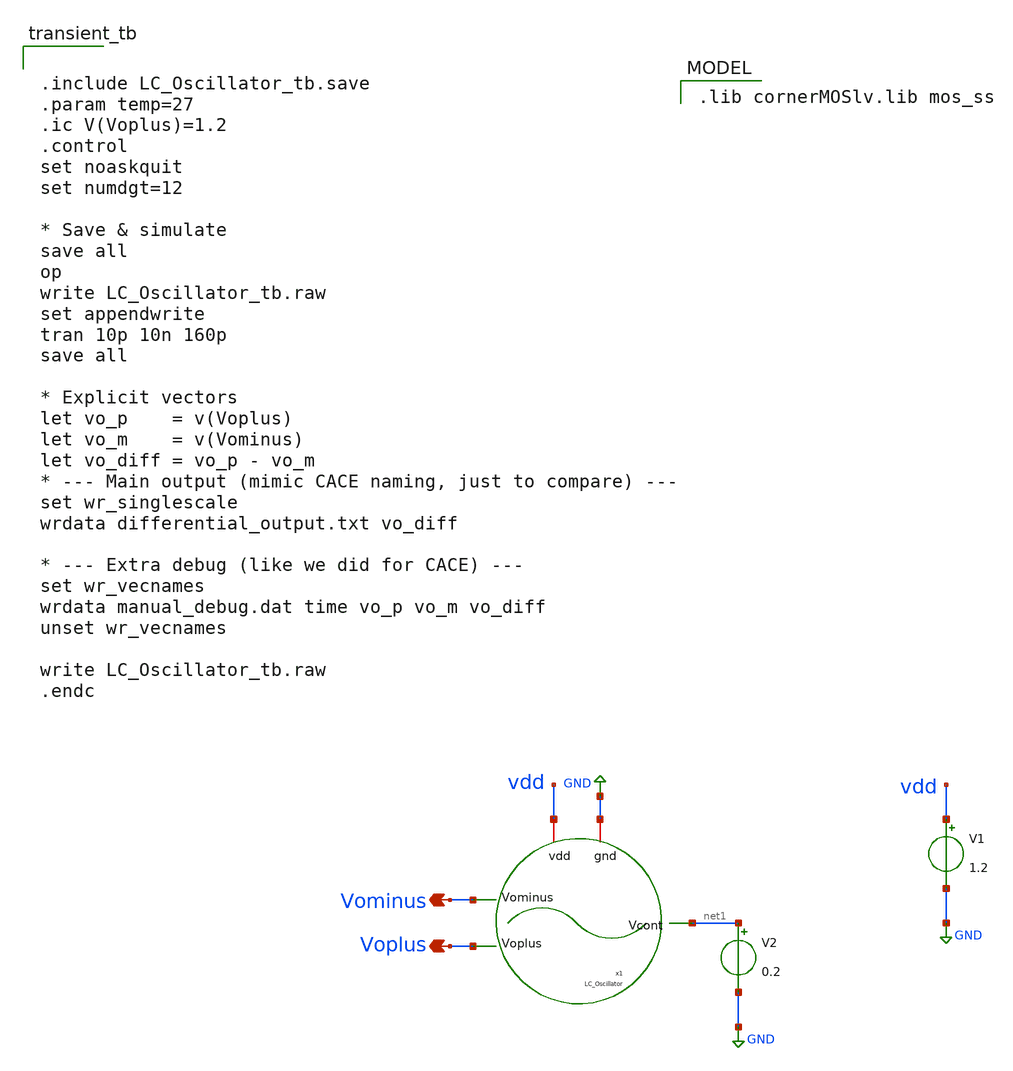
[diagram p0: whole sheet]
** sch_path: modules/module_4_type_2_PLL/LC_Oscillator/testbench/LC_Oscillator_tb.sch
**.subckt LC_Oscillator_tb Voplus Vominus
*.opin Voplus
*.opin Vominus
V1 vdd GND 1.2
x1 Voplus vdd GND Vominus net1 LC_Oscillator
V2 net1 GND 0.2
**** begin user architecture code


.include LC_Oscillator_tb.save
.param temp=27
.ic V(Voplus)=1.2
.control
set noaskquit
set numdgt=12

* Save & simulate
save all
op
write LC_Oscillator_tb.raw
set appendwrite
tran 10p 10n 160p
save all

* Explicit vectors
let vo_p    = v(Voplus)
let vo_m    = v(Vominus)
let vo_diff = vo_p - vo_m
* --- Main output (mimic CACE naming, just to compare) ---
set wr_singlescale
wrdata differential_output.txt vo_diff

* --- Extra debug (like we did for CACE) ---
set wr_vecnames
wrdata manual_debug.dat time vo_p vo_m vo_diff
unset wr_vecnames

write LC_Oscillator_tb.raw
.endc


 .lib cornerMOSlv.lib mos_ss

**** end user architecture code
**.ends

* expanding   symbol:  LC_Oscillator.sym # of pins=5
** sym_path: modules/module_4_type_2_PLL/LC_Oscillator/xschem/LC_Oscillator.sym
** sch_path: modules/module_4_type_2_PLL/LC_Oscillator/xschem/LC_Oscillator.sch
.subckt LC_Oscillator Voplus vdd gnd Vominus Vcont
*.iopin vdd
*.iopin gnd
*.opin Voplus
*.opin Vominus
*.ipin Vcont
XM1 Voplus Vominus net1 gnd sg13_lv_nmos w=16u l=0.13u ng=4 m=1 mm_ok=1
XM2 Vominus Voplus net1 gnd sg13_lv_nmos w=16u l=0.13u ng=4 m=1 mm_ok=1
R2 vdd Vominus 393 m=1
I0 net1 gnd 1m
L1 vdd Vominus 1.56n m=1
R1 vdd Voplus 393 m=1
L2 vdd Voplus 1.56n m=1
C1 Voplus gnd 300f m=1
C2 Vominus gnd 300f m=1
XM3 Vcont Voplus Vcont Vcont sg13_lv_nmos w=16u l=1u ng=4 m=1 mm_ok=1
XM4 Vcont Vominus Vcont Vcont sg13_lv_nmos w=16u l=1u ng=4 m=1 mm_ok=1
.ends

.GLOBAL GND
.end
